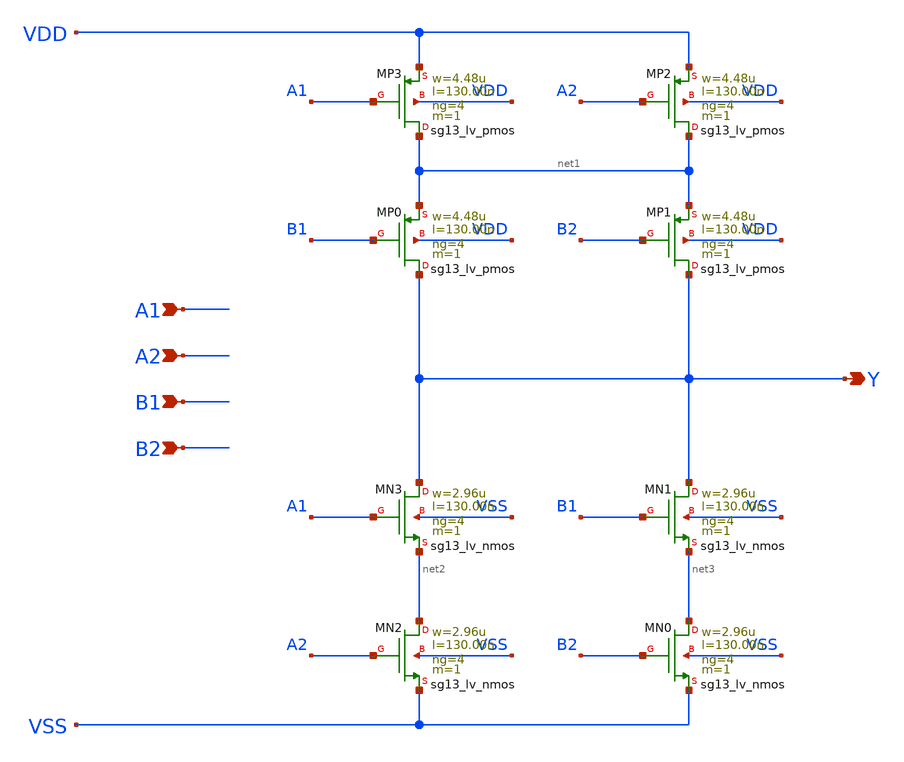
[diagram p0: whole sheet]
** sch_path: outputs/sg13g2_cells/cells/sg13g2_a22oi_4/sg13g2_a22oi_4.sch
**.subckt sg13g2_a22oi_4 A1 A2 B1 B2 Y
*.ipin A1
*.ipin A2
*.ipin B1
*.ipin B2
*.opin Y
XMN3 Y A1 net2 VSS sg13_lv_nmos w=2.96u l=130.00n ng=4 m=1 mm_ok=1
XMN2 net2 A2 VSS VSS sg13_lv_nmos w=2.96u l=130.00n ng=4 m=1 mm_ok=1
XMN1 Y B1 net3 VSS sg13_lv_nmos w=2.96u l=130.00n ng=4 m=1 mm_ok=1
XMN0 net3 B2 VSS VSS sg13_lv_nmos w=2.96u l=130.00n ng=4 m=1 mm_ok=1
XMP3 net1 A1 VDD VDD sg13_lv_pmos w=4.48u l=130.00n ng=4 m=1 mm_ok=1
XMP2 net1 A2 VDD VDD sg13_lv_pmos w=4.48u l=130.00n ng=4 m=1 mm_ok=1
XMP1 Y B2 net1 VDD sg13_lv_pmos w=4.48u l=130.00n ng=4 m=1 mm_ok=1
XMP0 Y B1 net1 VDD sg13_lv_pmos w=4.48u l=130.00n ng=4 m=1 mm_ok=1
**.ends
.end
